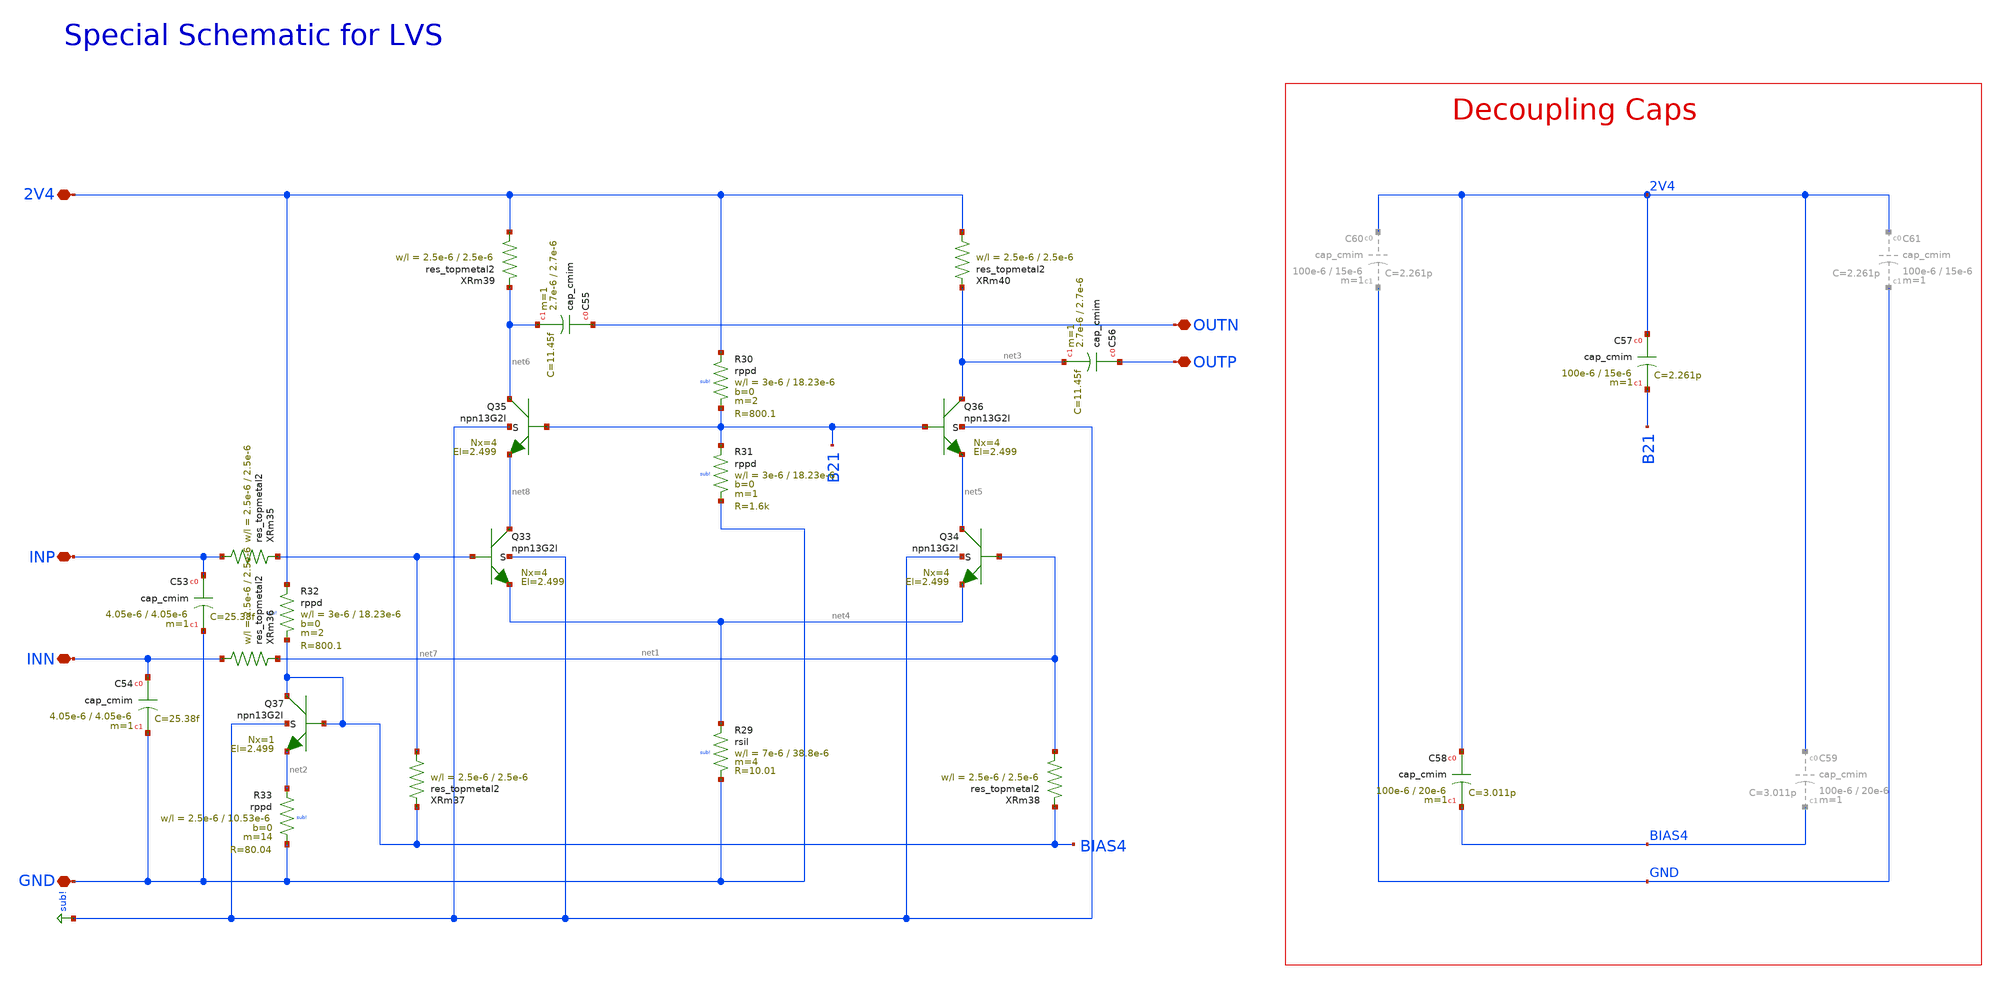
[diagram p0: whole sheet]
** sch_path: mWATTBAT/design_data/lvs/RXAMP_150GD_LVS.sch
**.subckt RXAMP_150GD_LVS 2V4 GND OUTN OUTP INP INN
*.iopin 2V4
*.iopin GND
*.iopin OUTN
*.iopin OUTP
*.iopin INP
*.iopin INN
XQ33 net8 net7 net4 sub! npn13G2l Nx=4 El=2.499 mm_ok=1
XQ34 net5 net1 net4 sub! npn13G2l Nx=4 El=2.499 mm_ok=1
XQ37 BIAS4 BIAS4 net2 sub! npn13G2l Nx=1 El=2.499 mm_ok=1
XQ35 net6 B21 net8 sub! npn13G2l Nx=4 El=2.499 mm_ok=1
XQ36 net3 B21 net5 sub! npn13G2l Nx=4 El=2.499 mm_ok=1
XR32 2V4 BIAS4 sub! rppd w=3e-6 l=18.23e-6 m=2 b=0 mm_ok=1
XC53 INP GND cap_cmim w=4.05e-6 l=4.05e-6 m=1 mm_ok=1
XC54 INN GND cap_cmim w=4.05e-6 l=4.05e-6 m=1 mm_ok=1
XC55 OUTN net6 cap_cmim w=2.7e-6 l=2.7e-6 m=1 mm_ok=1
XC56 OUTP net3 cap_cmim w=2.7e-6 l=2.7e-6 m=1 mm_ok=1
XR33 net2 GND sub! rppd w=2.5e-6 l=10.53e-6 m=14 b=0 mm_ok=1
XR30 2V4 B21 sub! rppd w=3e-6 l=18.23e-6 m=2 b=0 mm_ok=1
XR31 B21 GND sub! rppd w=3e-6 l=18.23e-6 m=1 b=0 mm_ok=1
XC58 2V4 BIAS4 cap_cmim w=100e-6 l=20e-6 m=1 mm_ok=1
XC57 2V4 B21 cap_cmim w=100e-6 l=15e-6 m=1 mm_ok=1
XR29 net4 GND sub! rsil w=7e-6 l=38.8e-6 m=4 mm_ok=1
XRm35 INP net7 res_topmetal2 w=2.5e-6 l=2.5e-6
XRm36 INN net1 res_topmetal2 w=2.5e-6 l=2.5e-6
XRm37 net7 BIAS4 res_topmetal2 w=2.5e-6 l=2.5e-6
XRm38 net1 BIAS4 res_topmetal2 w=2.5e-6 l=2.5e-6
XRm39 2V4 net6 res_topmetal2 w=2.5e-6 l=2.5e-6
XRm40 2V4 net3 res_topmetal2 w=2.5e-6 l=2.5e-6
**.ends
.GLOBAL sub!
.end
